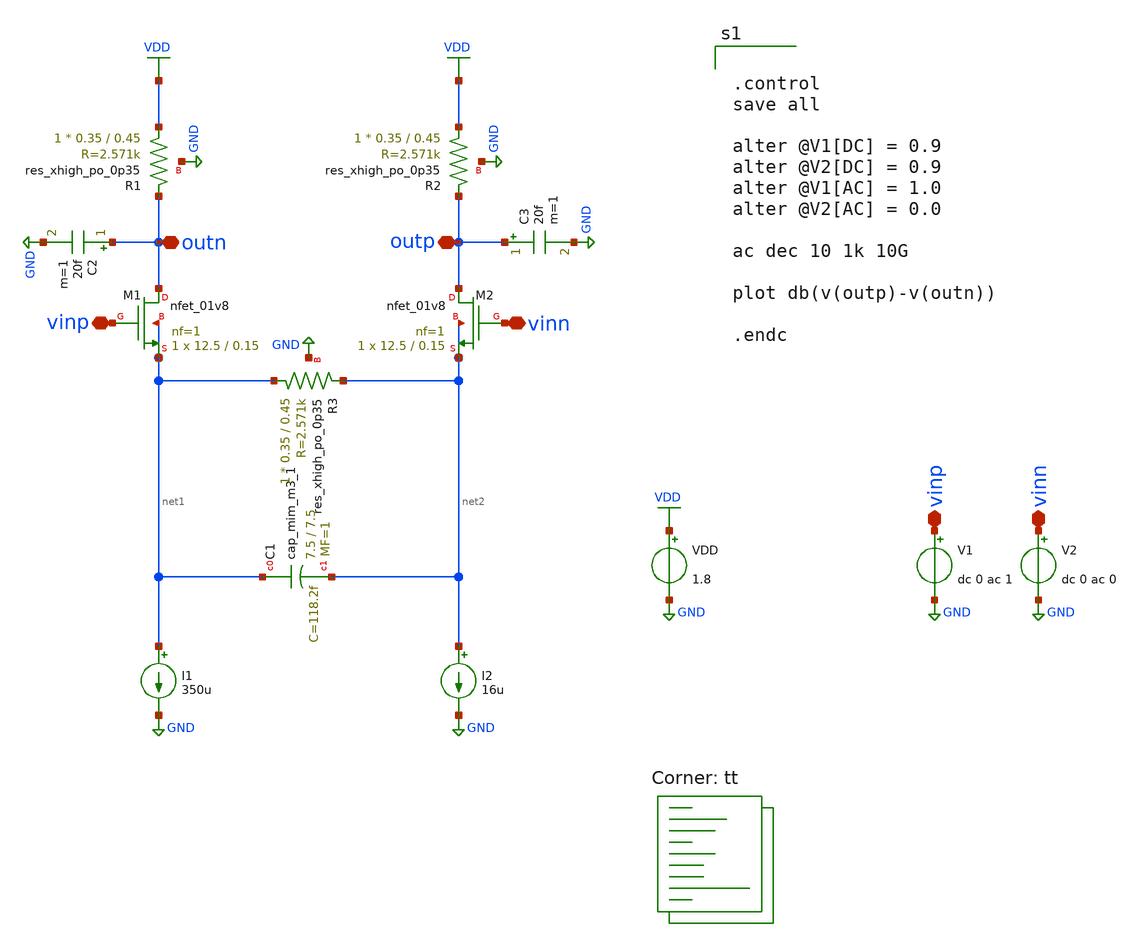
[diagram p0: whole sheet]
** sch_path: CTLE/Old_Design/tb_ctle-base.sch
**.subckt tb_ctle-base vinp vinn vinp vinn outn outp
*.iopin vinp
*.iopin vinn
*.iopin vinp
*.iopin vinn
*.iopin outn
*.iopin outp
XM1 outn vinp net1 net1 sky130_fd_pr__nfet_01v8 L=0.15 W=12.5 nf=1 ad='int((nf+1)/2) * W/nf * 0.29' as='int((nf+2)/2) * W/nf * 0.29'
+ pd='2*int((nf+1)/2) * (W/nf + 0.29)' ps='2*int((nf+2)/2) * (W/nf + 0.29)' nrd='0.29 / W' nrs='0.29 / W'
+ sa=0 sb=0 sd=0 mult=1 m=1
XM2 outp vinn net2 net2 sky130_fd_pr__nfet_01v8 L=0.15 W=12.5 nf=1 ad='int((nf+1)/2) * W/nf * 0.29' as='int((nf+2)/2) * W/nf * 0.29'
+ pd='2*int((nf+1)/2) * (W/nf + 0.29)' ps='2*int((nf+2)/2) * (W/nf + 0.29)' nrd='0.29 / W' nrs='0.29 / W'
+ sa=0 sb=0 sd=0 mult=1 m=1
XC1 net1 net2 sky130_fd_pr__cap_mim_m3_1 W=7.5 L=7.5 MF=1 m=1
XR3 net1 net2 GND sky130_fd_pr__res_xhigh_po_0p35 L=0.45 mult=1 m=1
XR1 VDD outn GND sky130_fd_pr__res_xhigh_po_0p35 L=0.45 mult=1 m=1
XR2 VDD outp GND sky130_fd_pr__res_xhigh_po_0p35 L=0.45 mult=1 m=1
VDD VDD GND 1.8
V1 vinp GND dc 0 ac 1
V2 vinn GND dc 0 ac 0
I1 net1 GND 350u
I2 net2 GND 16u
C2 outn GND 20f m=1
C3 outp GND 20f m=1
**** begin user architecture code
.lib $::SKYWATER_MODELS/sky130.lib.spice tt


.control
save all

alter @V1[DC] = 0.9
alter @V2[DC] = 0.9
alter @V1[AC] = 1.0
alter @V2[AC] = 0.0

ac dec 10 1k 10G

plot db(v(outp)-v(outn))

.endc

**** end user architecture code
**.ends
.GLOBAL GND
.GLOBAL VDD
.end
